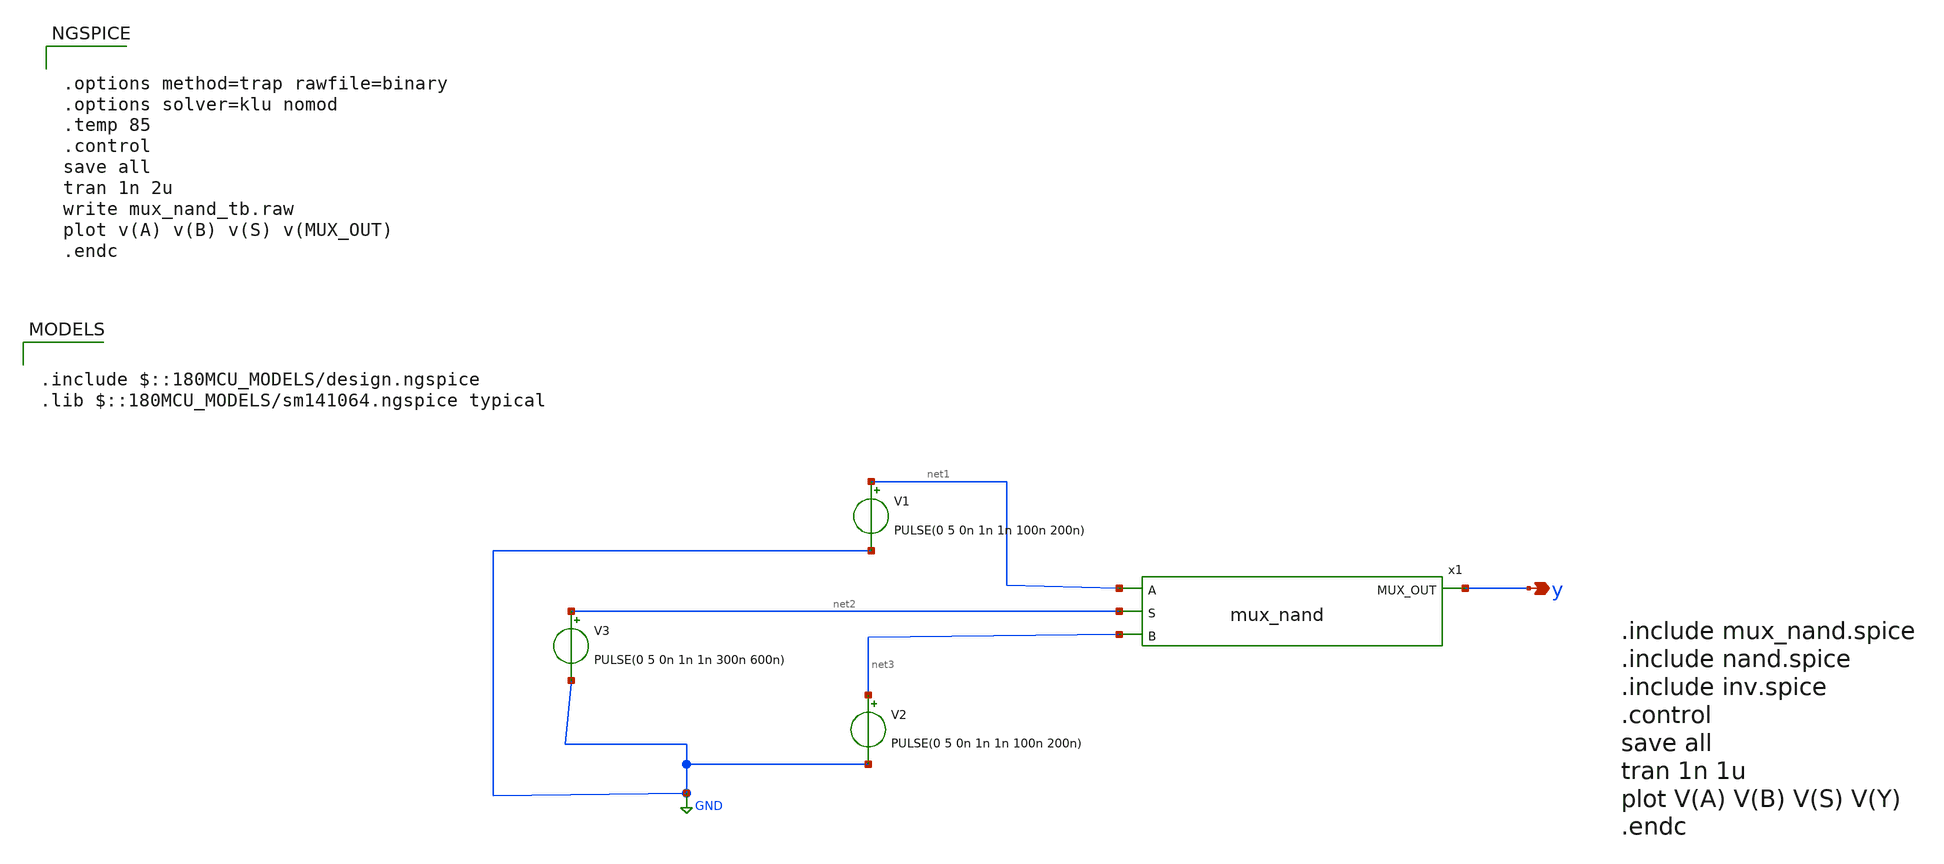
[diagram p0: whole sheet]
** sch_path: designs/schematics/mux2x1/mux_nand_tb.sch
**.subckt mux_nand_tb y
*.opin y
V1 net1 GND PULSE(0 5 0n 1n 1n 100n 200n)
V2 net4 GND PULSE(0 5 0n 1n 1n 100n 200n)
V3 net2 GND PULSE(0 5 0n 1n 1n 300n 600n)
x1 net1 y net2 net3 mux_nand
**** begin user architecture code

.include $::180MCU_MODELS/design.ngspice
.lib $::180MCU_MODELS/sm141064.ngspice typical



.options method=trap rawfile=binary
.options solver=klu nomod
.temp 85
.control
save all
tran 1n 2u
write mux_nand_tb.raw
plot v(A) v(B) v(S) v(MUX_OUT)
.endc


**** end user architecture code
**.ends

* expanding   symbol:  voidwalkers-scandff-gf180mcu/designs/schematics/mux2x1/mux_nand.sym # of
*+ pins=4
** sym_path: designs/schematics/mux2x1/mux_nand.sym
** sch_path: designs/schematics/mux2x1/mux_nand.sch
.subckt mux_nand A MUX_OUT S B
*.ipin S
*.ipin A
*.ipin B
*.opin MUX_OUT
x1 VDD S net1 GND inv
x2 A net1 net2 nand
x3 B net1 net3 nand
x4 net2 net3 MUX_OUT nand
.ends


* expanding   symbol:  voidwalkers-scandff-gf180mcu/designs/schematics/mux2x1/inv.sym # of pins=4
** sym_path: designs/schematics/mux2x1/inv.sym
** sch_path: designs/schematics/mux2x1/inv.sch
.subckt inv vcc in out gnd
*.ipin in
*.opin out
*.iopin vcc
*.iopin gnd
XM2 out in vcc vcc pfet_03v3 L=0.28u W=0.22u nf=1 ad='int((nf+1)/2) * W/nf * 0.18u' as='int((nf+2)/2) * W/nf * 0.18u'
+ pd='2*int((nf+1)/2) * (W/nf + 0.18u)' ps='2*int((nf+2)/2) * (W/nf + 0.18u)' nrd='0.18u / W' nrs='0.18u / W'
+ sa=0 sb=0 sd=0 m=1
XM1 out in gnd gnd nfet_03v3 L=0.28u W=0.22u nf=1 ad='int((nf+1)/2) * W/nf * 0.18u' as='int((nf+2)/2) * W/nf * 0.18u'
+ pd='2*int((nf+1)/2) * (W/nf + 0.18u)' ps='2*int((nf+2)/2) * (W/nf + 0.18u)' nrd='0.18u / W' nrs='0.18u / W'
+ sa=0 sb=0 sd=0 m=1
.ends


* expanding   symbol:  voidwalkers-scandff-gf180mcu/designs/schematics/mux2x1/nand.sym # of pins=3
** sym_path: designs/schematics/mux2x1/nand.sym
** sch_path: designs/schematics/mux2x1/nand.sch
.subckt nand A B OUT
*.ipin B
*.ipin A
*.opin OUT
XM1 OUT A net1 GND nfet_03v3 L=0.28u W=0.22u nf=1 ad='int((nf+1)/2) * W/nf * 0.18u' as='int((nf+2)/2) * W/nf * 0.18u'
+ pd='2*int((nf+1)/2) * (W/nf + 0.18u)' ps='2*int((nf+2)/2) * (W/nf + 0.18u)' nrd='0.18u / W' nrs='0.18u / W'
+ sa=0 sb=0 sd=0 m=1
XM2 net1 B GND GND nfet_03v3 L=0.28u W=0.22u nf=1 ad='int((nf+1)/2) * W/nf * 0.18u' as='int((nf+2)/2) * W/nf * 0.18u'
+ pd='2*int((nf+1)/2) * (W/nf + 0.18u)' ps='2*int((nf+2)/2) * (W/nf + 0.18u)' nrd='0.18u / W' nrs='0.18u / W'
+ sa=0 sb=0 sd=0 m=1
XM3 OUT A VDD VDD pfet_03v3 L=0.28u W=0.22u nf=1 ad='int((nf+1)/2) * W/nf * 0.18u' as='int((nf+2)/2) * W/nf * 0.18u'
+ pd='2*int((nf+1)/2) * (W/nf + 0.18u)' ps='2*int((nf+2)/2) * (W/nf + 0.18u)' nrd='0.18u / W' nrs='0.18u / W'
+ sa=0 sb=0 sd=0 m=1
XM4 OUT B VDD VDD pfet_03v3 L=0.28u W=0.22u nf=1 ad='int((nf+1)/2) * W/nf * 0.18u' as='int((nf+2)/2) * W/nf * 0.18u'
+ pd='2*int((nf+1)/2) * (W/nf + 0.18u)' ps='2*int((nf+2)/2) * (W/nf + 0.18u)' nrd='0.18u / W' nrs='0.18u / W'
+ sa=0 sb=0 sd=0 m=1
.ends

.GLOBAL GND
.GLOBAL VDD
.end
